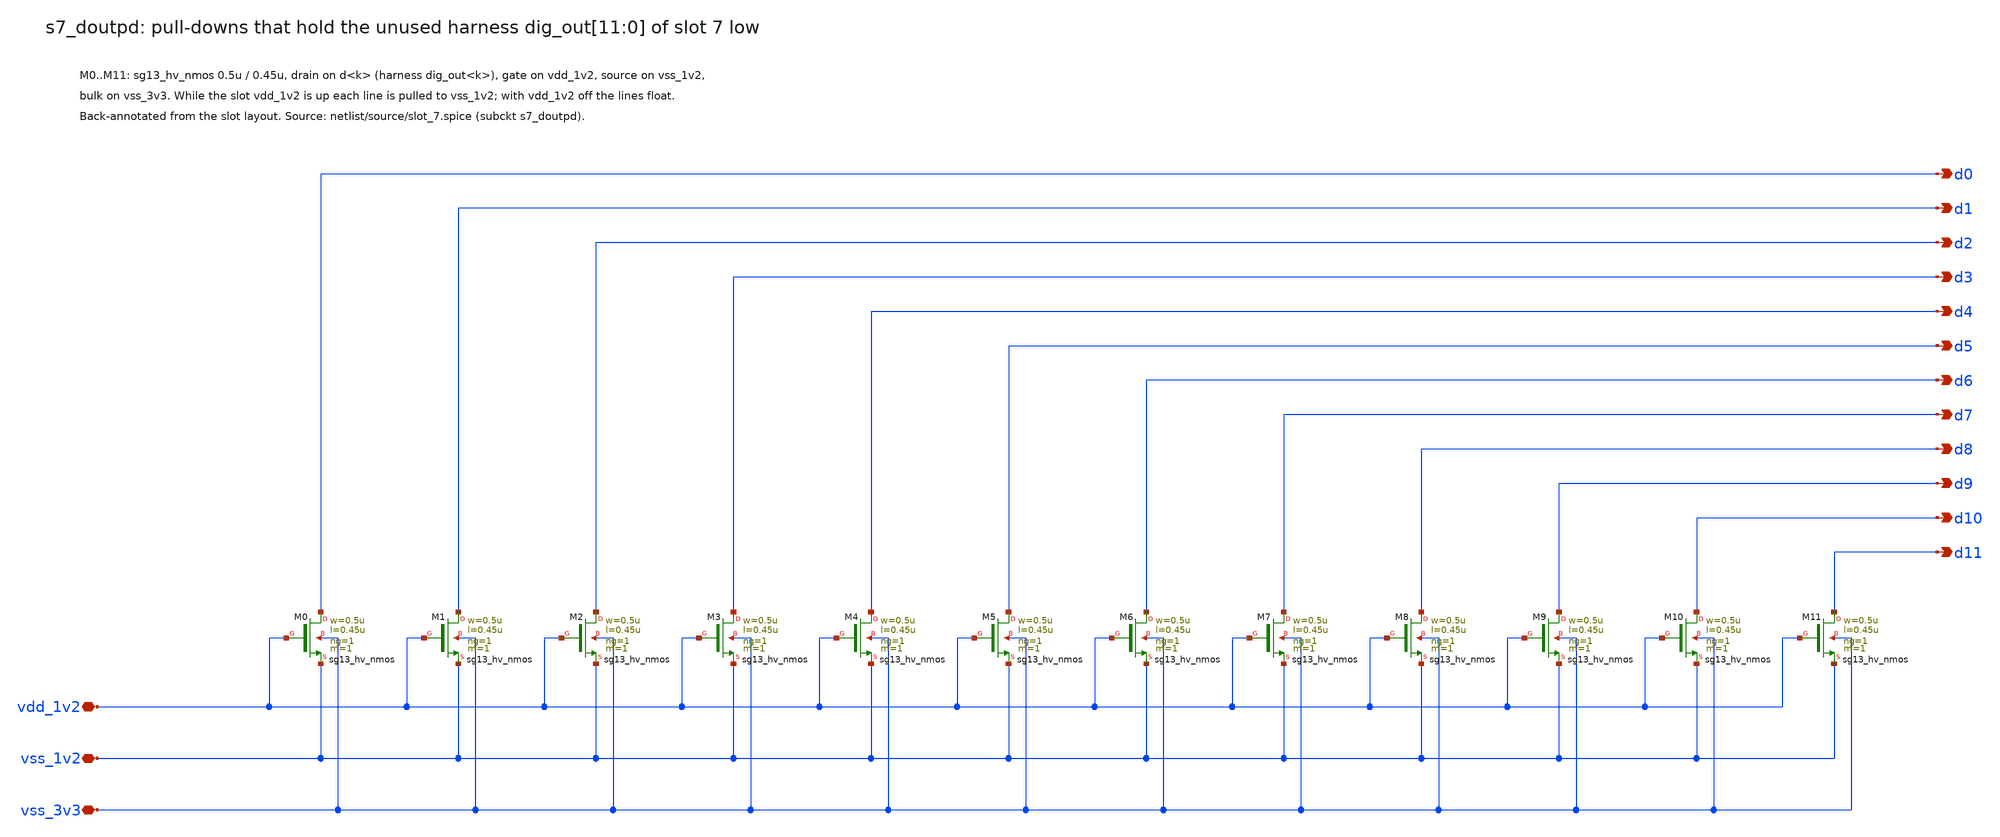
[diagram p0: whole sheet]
** sch_path: macros/slot_7/schematic/xschem/s7_doutpd.sch
**.subckt s7_doutpd d0 d1 d2 d3 d4 d5 d6 d7 d8 d9 d10 d11 vdd_1v2 vss_1v2 vss_3v3
*.opin d0
*.opin d1
*.opin d2
*.opin d3
*.opin d4
*.opin d5
*.opin d6
*.opin d7
*.opin d8
*.opin d9
*.opin d10
*.opin d11
*.iopin vdd_1v2
*.iopin vss_1v2
*.iopin vss_3v3
XM0 d0 vdd_1v2 vss_1v2 vss_3v3 sg13_hv_nmos w=0.5u l=0.45u ng=1 m=1 mm_ok=1
XM1 d1 vdd_1v2 vss_1v2 vss_3v3 sg13_hv_nmos w=0.5u l=0.45u ng=1 m=1 mm_ok=1
XM2 d2 vdd_1v2 vss_1v2 vss_3v3 sg13_hv_nmos w=0.5u l=0.45u ng=1 m=1 mm_ok=1
XM3 d3 vdd_1v2 vss_1v2 vss_3v3 sg13_hv_nmos w=0.5u l=0.45u ng=1 m=1 mm_ok=1
XM4 d4 vdd_1v2 vss_1v2 vss_3v3 sg13_hv_nmos w=0.5u l=0.45u ng=1 m=1 mm_ok=1
XM5 d5 vdd_1v2 vss_1v2 vss_3v3 sg13_hv_nmos w=0.5u l=0.45u ng=1 m=1 mm_ok=1
XM6 d6 vdd_1v2 vss_1v2 vss_3v3 sg13_hv_nmos w=0.5u l=0.45u ng=1 m=1 mm_ok=1
XM7 d7 vdd_1v2 vss_1v2 vss_3v3 sg13_hv_nmos w=0.5u l=0.45u ng=1 m=1 mm_ok=1
XM8 d8 vdd_1v2 vss_1v2 vss_3v3 sg13_hv_nmos w=0.5u l=0.45u ng=1 m=1 mm_ok=1
XM9 d9 vdd_1v2 vss_1v2 vss_3v3 sg13_hv_nmos w=0.5u l=0.45u ng=1 m=1 mm_ok=1
XM10 d10 vdd_1v2 vss_1v2 vss_3v3 sg13_hv_nmos w=0.5u l=0.45u ng=1 m=1 mm_ok=1
XM11 d11 vdd_1v2 vss_1v2 vss_3v3 sg13_hv_nmos w=0.5u l=0.45u ng=1 m=1 mm_ok=1
**.ends
.end
